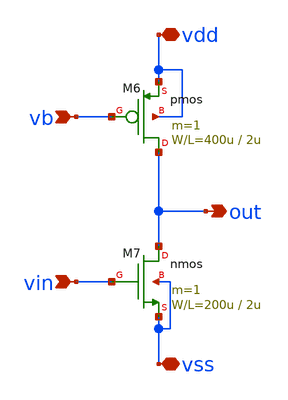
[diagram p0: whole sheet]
** sch_path: OR1/PTC06/opamp/cs.sch
**.subckt cs vb vin out vss vdd
*.ipin vb
*.ipin vin
*.opin out
*.iopin vss
*.iopin vdd
M6 out vb vdd vdd pmos L=2u W=400u m=1
M7 out vin vss vss nmos L=2u W=200u m=1
**.ends
.end
